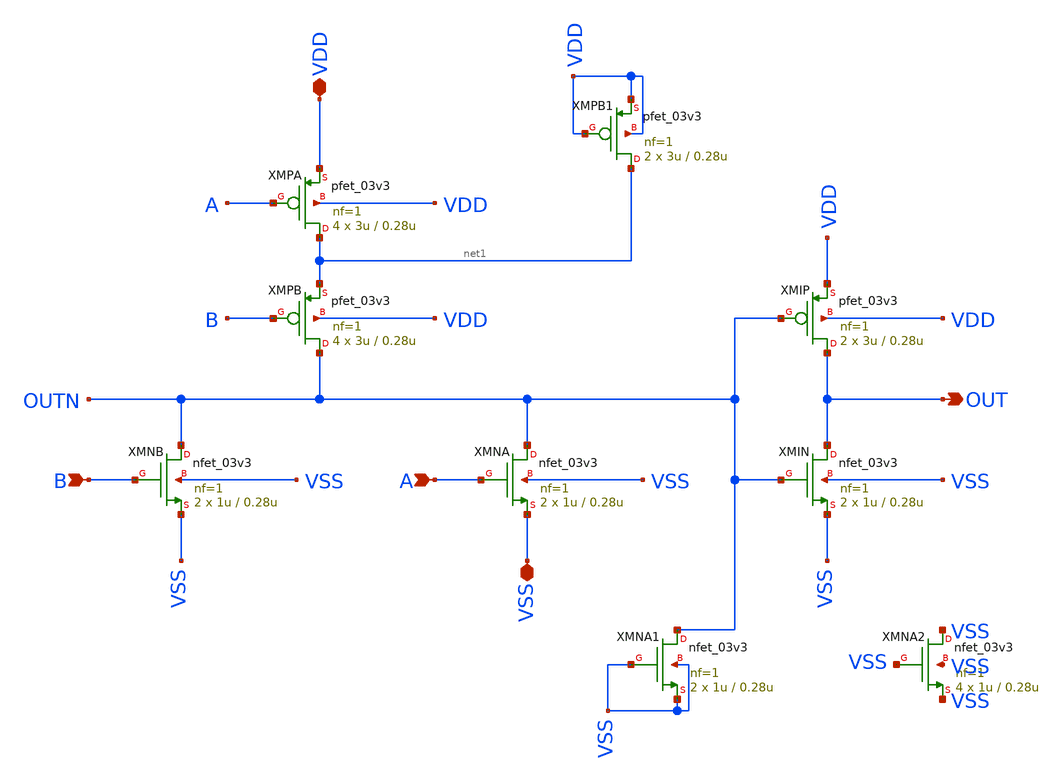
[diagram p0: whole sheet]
** sch_path: designs/DS_modulator/gate_or/xschem/gate_or.sch
**.subckt gate_or OUT A VDD VSS B
*.opin OUT
*.ipin A
*.iopin VDD
*.iopin VSS
*.ipin B
XMNB OUTN B VSS VSS nfet_03v3 L=0.28u W=1u nf=1 ad='int((nf+1)/2) * W/nf * 0.18u' as='int((nf+2)/2) * W/nf * 0.18u'
+ pd='2*int((nf+1)/2) * (W/nf + 0.18u)' ps='2*int((nf+2)/2) * (W/nf + 0.18u)' nrd='0.18u / W' nrs='0.18u / W'
+ sa=0 sb=0 sd=0 m=2
XMPB OUTN B net1 VDD pfet_03v3 L=0.28u W=3u nf=1 ad='int((nf+1)/2) * W/nf * 0.18u' as='int((nf+2)/2) * W/nf * 0.18u'
+ pd='2*int((nf+1)/2) * (W/nf + 0.18u)' ps='2*int((nf+2)/2) * (W/nf + 0.18u)' nrd='0.18u / W' nrs='0.18u / W'
+ sa=0 sb=0 sd=0 m=4
XMNA OUTN A VSS VSS nfet_03v3 L=0.28u W=1u nf=1 ad='int((nf+1)/2) * W/nf * 0.18u' as='int((nf+2)/2) * W/nf * 0.18u'
+ pd='2*int((nf+1)/2) * (W/nf + 0.18u)' ps='2*int((nf+2)/2) * (W/nf + 0.18u)' nrd='0.18u / W' nrs='0.18u / W'
+ sa=0 sb=0 sd=0 m=2
XMPA net1 A VDD VDD pfet_03v3 L=0.28u W=3u nf=1 ad='int((nf+1)/2) * W/nf * 0.18u' as='int((nf+2)/2) * W/nf * 0.18u'
+ pd='2*int((nf+1)/2) * (W/nf + 0.18u)' ps='2*int((nf+2)/2) * (W/nf + 0.18u)' nrd='0.18u / W' nrs='0.18u / W'
+ sa=0 sb=0 sd=0 m=4
XMIN OUT OUTN VSS VSS nfet_03v3 L=0.28u W=1u nf=1 ad='int((nf+1)/2) * W/nf * 0.18u' as='int((nf+2)/2) * W/nf * 0.18u'
+ pd='2*int((nf+1)/2) * (W/nf + 0.18u)' ps='2*int((nf+2)/2) * (W/nf + 0.18u)' nrd='0.18u / W' nrs='0.18u / W'
+ sa=0 sb=0 sd=0 m=2
XMIP OUT OUTN VDD VDD pfet_03v3 L=0.28u W=3u nf=1 ad='int((nf+1)/2) * W/nf * 0.18u' as='int((nf+2)/2) * W/nf * 0.18u'
+ pd='2*int((nf+1)/2) * (W/nf + 0.18u)' ps='2*int((nf+2)/2) * (W/nf + 0.18u)' nrd='0.18u / W' nrs='0.18u / W'
+ sa=0 sb=0 sd=0 m=2
XMPB1 net1 VDD VDD VDD pfet_03v3 L=0.28u W=3u nf=1 ad='int((nf+1)/2) * W/nf * 0.18u' as='int((nf+2)/2) * W/nf * 0.18u'
+ pd='2*int((nf+1)/2) * (W/nf + 0.18u)' ps='2*int((nf+2)/2) * (W/nf + 0.18u)' nrd='0.18u / W' nrs='0.18u / W'
+ sa=0 sb=0 sd=0 m=2
XMNA1 OUTN VSS VSS VSS nfet_03v3 L=0.28u W=1u nf=1 ad='int((nf+1)/2) * W/nf * 0.18u' as='int((nf+2)/2) * W/nf * 0.18u'
+ pd='2*int((nf+1)/2) * (W/nf + 0.18u)' ps='2*int((nf+2)/2) * (W/nf + 0.18u)' nrd='0.18u / W' nrs='0.18u / W'
+ sa=0 sb=0 sd=0 m=2
XMNA2 VSS VSS VSS VSS nfet_03v3 L=0.28u W=1u nf=1 ad='int((nf+1)/2) * W/nf * 0.18u' as='int((nf+2)/2) * W/nf * 0.18u'
+ pd='2*int((nf+1)/2) * (W/nf + 0.18u)' ps='2*int((nf+2)/2) * (W/nf + 0.18u)' nrd='0.18u / W' nrs='0.18u / W'
+ sa=0 sb=0 sd=0 m=4
**.ends
.end
